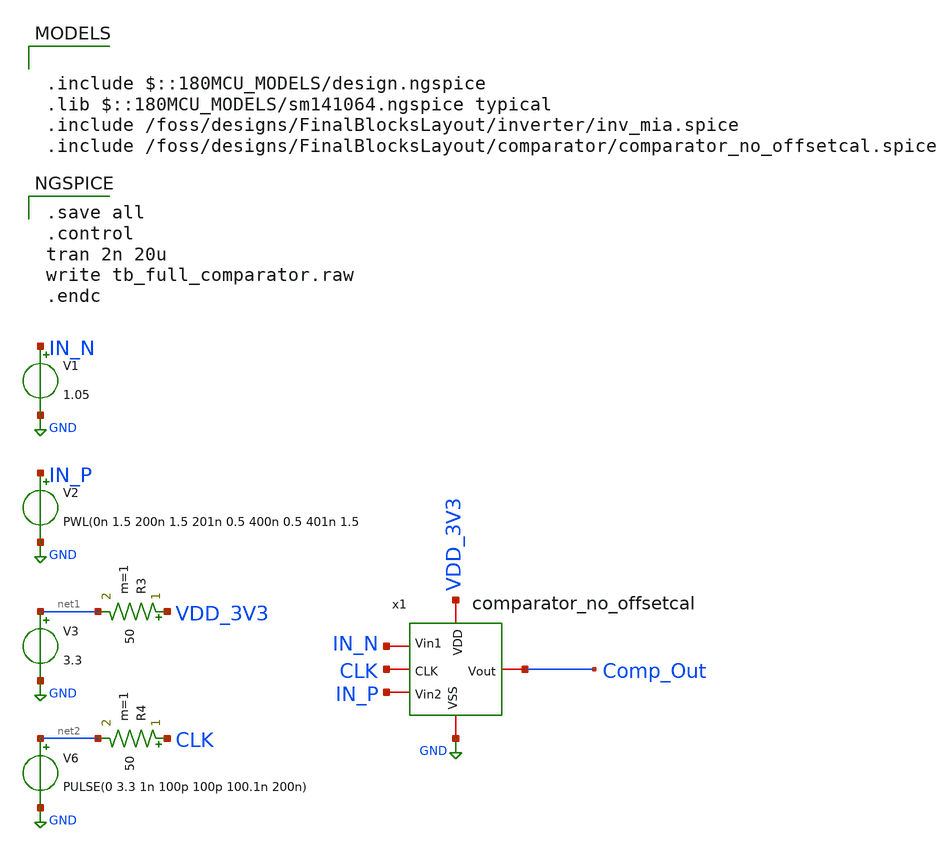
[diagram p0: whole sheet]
** sch_path: designs/FinalBlocksLayout/comparator/tb_full_comparator.sch
**.subckt tb_full_comparator
V3 net1 GND 3.3
V6 net2 GND PULSE(0 3.3 1n 100p 100p 100.1n 200n)
R3 VDD_3V3 net1 50 m=1
R4 CLK net2 50 m=1
V2 IN_P GND PWL(0n 1.5 200n 1.5 201n 0.5 400n 0.5 401n 1.5
V1 IN_N GND 1.05
x1 VDD_3V3 GND CLK IN_N IN_P Comp_Out comparator_no_offsetcal
**** begin user architecture code

.include $::180MCU_MODELS/design.ngspice
.lib $::180MCU_MODELS/sm141064.ngspice typical
.include /foss/designs/FinalBlocksLayout/inverter/inv_mia.spice
.include /foss/designs/FinalBlocksLayout/comparator/comparator_no_offsetcal.spice


.save all
.control
tran 2n 20u
write tb_full_comparator.raw
.endc

**** end user architecture code
**.ends
.GLOBAL GND
.end
